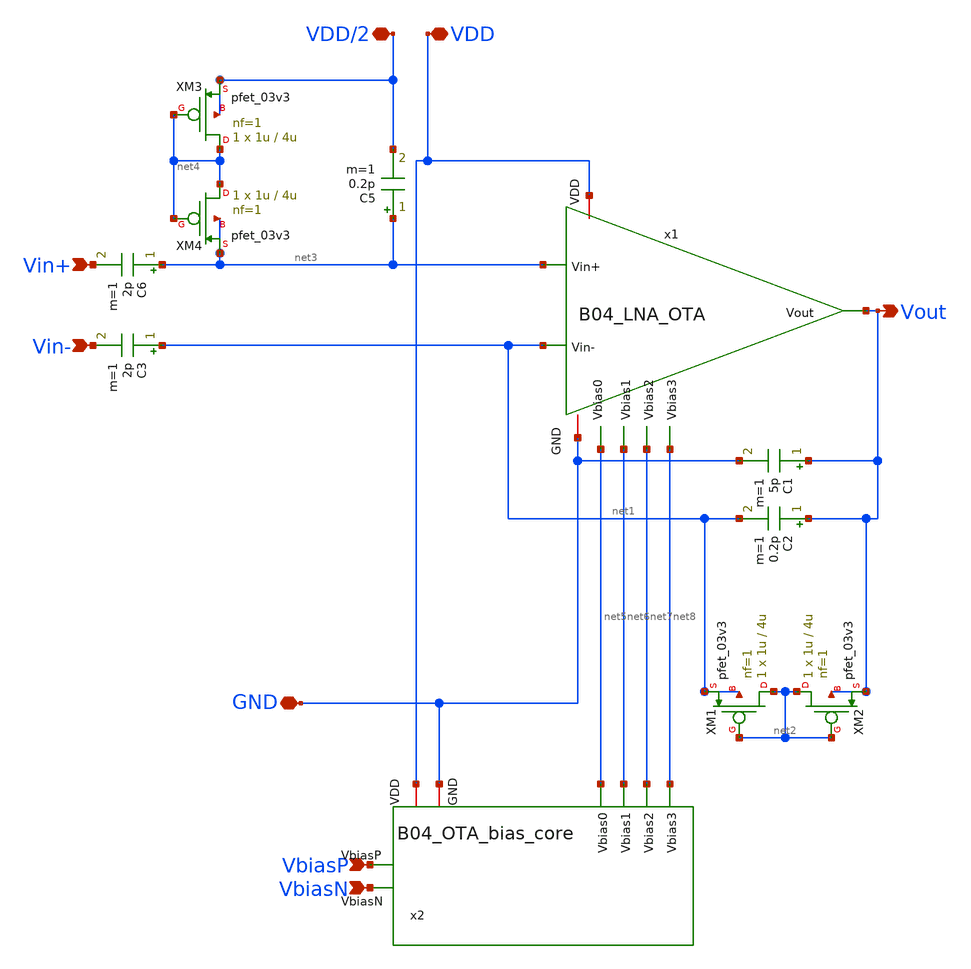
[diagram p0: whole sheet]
** sch_path: analog/B04_LNA.sch
**.subckt B04_LNA VDD VDD/2 GND Vin+ Vin- VbiasP Vout VbiasN
*.iopin VDD
*.iopin VDD/2
*.iopin GND
*.ipin Vin+
*.ipin Vin-
*.ipin VbiasP
*.opin Vout
*.ipin VbiasN
C2 Vout net1 0.2p m=1
C3 net1 Vin- 2p m=1
C5 net3 VDD/2 0.2p m=1
XM1 net2 net2 net1 net1 pfet_03v3 L=4u W=1u nf=1 ad='int((nf+1)/2) * W/nf * 0.18u' as='int((nf+2)/2) * W/nf * 0.18u'
+ pd='2*int((nf+1)/2) * (W/nf + 0.18u)' ps='2*int((nf+2)/2) * (W/nf + 0.18u)' nrd='0.18u / W' nrs='0.18u / W'
+ sa=0 sb=0 sd=0 m=1
XM2 net2 net2 Vout Vout pfet_03v3 L=4u W=1u nf=1 ad='int((nf+1)/2) * W/nf * 0.18u' as='int((nf+2)/2) * W/nf * 0.18u'
+ pd='2*int((nf+1)/2) * (W/nf + 0.18u)' ps='2*int((nf+2)/2) * (W/nf + 0.18u)' nrd='0.18u / W' nrs='0.18u / W'
+ sa=0 sb=0 sd=0 m=1
XM3 net4 net4 VDD/2 VDD/2 pfet_03v3 L=4u W=1u nf=1 ad='int((nf+1)/2) * W/nf * 0.18u' as='int((nf+2)/2) * W/nf * 0.18u'
+ pd='2*int((nf+1)/2) * (W/nf + 0.18u)' ps='2*int((nf+2)/2) * (W/nf + 0.18u)' nrd='0.18u / W' nrs='0.18u / W'
+ sa=0 sb=0 sd=0 m=1
XM4 net4 net4 net3 net3 pfet_03v3 L=4u W=1u nf=1 ad='int((nf+1)/2) * W/nf * 0.18u' as='int((nf+2)/2) * W/nf * 0.18u'
+ pd='2*int((nf+1)/2) * (W/nf + 0.18u)' ps='2*int((nf+2)/2) * (W/nf + 0.18u)' nrd='0.18u / W' nrs='0.18u / W'
+ sa=0 sb=0 sd=0 m=1
C6 net3 Vin+ 2p m=1
x1 VDD net5 net3 net1 net8 net6 Vout net7 GND B04_LNA_OTA
x2 VDD VbiasP net5 net7 net8 net6 VbiasN GND B04_OTA_bias_core ratio=8
C1 Vout GND 5p m=1
**.ends

* expanding   symbol:
*+  AURA-Event-Driven-Mixed-Signal-ASIC-for-Acoustic-Pattern-Detection/analog/B04_LNA_OTA.sym # of pins=9
** sym_path: analog/B04_LNA_OTA.sym
** sch_path: analog/B04_LNA_OTA.sch
.subckt B04_LNA_OTA VDD Vbias0 Vin+ Vin- Vbias3 Vbias1 Vout Vbias2 GND
*.iopin VDD
*.ipin Vbias0
*.ipin Vin+
*.ipin Vin-
*.opin Vout
*.ipin Vbias3
*.ipin Vbias2
*.iopin GND
*.ipin Vbias1
XM1 net1 Vbias0 VDD VDD pfet_03v3 L=4u W=5u nf=2 ad='int((nf+1)/2) * W/nf * 0.18u' as='int((nf+2)/2) * W/nf * 0.18u'
+ pd='2*int((nf+1)/2) * (W/nf + 0.18u)' ps='2*int((nf+2)/2) * (W/nf + 0.18u)' nrd='0.18u / W' nrs='0.18u / W'
+ sa=0 sb=0 sd=0 m=1
XM2 net6 Vin+ net1 VDD pfet_03v3 L=8u W=16u nf=9 ad='int((nf+1)/2) * W/nf * 0.18u' as='int((nf+2)/2) * W/nf * 0.18u'
+ pd='2*int((nf+1)/2) * (W/nf + 0.18u)' ps='2*int((nf+2)/2) * (W/nf + 0.18u)' nrd='0.18u / W' nrs='0.18u / W'
+ sa=0 sb=0 sd=0 m=1
XM3 net7 Vin- net1 VDD pfet_03v3 L=8u W=16u nf=9 ad='int((nf+1)/2) * W/nf * 0.18u' as='int((nf+2)/2) * W/nf * 0.18u'
+ pd='2*int((nf+1)/2) * (W/nf + 0.18u)' ps='2*int((nf+2)/2) * (W/nf + 0.18u)' nrd='0.18u / W' nrs='0.18u / W'
+ sa=0 sb=0 sd=0 m=1
XM4 net2 Vin+ net1 VDD pfet_03v3 L=8u W=16u nf=1 ad='int((nf+1)/2) * W/nf * 0.18u' as='int((nf+2)/2) * W/nf * 0.18u'
+ pd='2*int((nf+1)/2) * (W/nf + 0.18u)' ps='2*int((nf+2)/2) * (W/nf + 0.18u)' nrd='0.18u / W' nrs='0.18u / W'
+ sa=0 sb=0 sd=0 m=1
XM5 net3 Vin- net1 VDD pfet_03v3 L=8u W=16u nf=1 ad='int((nf+1)/2) * W/nf * 0.18u' as='int((nf+2)/2) * W/nf * 0.18u'
+ pd='2*int((nf+1)/2) * (W/nf + 0.18u)' ps='2*int((nf+2)/2) * (W/nf + 0.18u)' nrd='0.18u / W' nrs='0.18u / W'
+ sa=0 sb=0 sd=0 m=1
XM6 net2 Vbias2 net5 0 nfet_03v3 L=2u W=4u nf=1 ad='int((nf+1)/2) * W/nf * 0.18u' as='int((nf+2)/2) * W/nf * 0.18u'
+ pd='2*int((nf+1)/2) * (W/nf + 0.18u)' ps='2*int((nf+2)/2) * (W/nf + 0.18u)' nrd='0.18u / W' nrs='0.18u / W'
+ sa=0 sb=0 sd=0 m=1
XM7 net3 Vbias2 net4 0 nfet_03v3 L=2u W=4u nf=1 ad='int((nf+1)/2) * W/nf * 0.18u' as='int((nf+2)/2) * W/nf * 0.18u'
+ pd='2*int((nf+1)/2) * (W/nf + 0.18u)' ps='2*int((nf+2)/2) * (W/nf + 0.18u)' nrd='0.18u / W' nrs='0.18u / W'
+ sa=0 sb=0 sd=0 m=1
XM8 net5 net2 GND GND nfet_03v3 L=8u W=2u nf=1 ad='int((nf+1)/2) * W/nf * 0.18u' as='int((nf+2)/2) * W/nf * 0.18u'
+ pd='2*int((nf+1)/2) * (W/nf + 0.18u)' ps='2*int((nf+2)/2) * (W/nf + 0.18u)' nrd='0.18u / W' nrs='0.18u / W'
+ sa=0 sb=0 sd=0 m=1
XM9 net6 net3 GND GND nfet_03v3 L=8u W=2u nf=1 ad='int((nf+1)/2) * W/nf * 0.18u' as='int((nf+2)/2) * W/nf * 0.18u'
+ pd='2*int((nf+1)/2) * (W/nf + 0.18u)' ps='2*int((nf+2)/2) * (W/nf + 0.18u)' nrd='0.18u / W' nrs='0.18u / W'
+ sa=0 sb=0 sd=0 m=1
XM10 net4 net3 GND GND nfet_03v3 L=8u W=2u nf=1 ad='int((nf+1)/2) * W/nf * 0.18u' as='int((nf+2)/2) * W/nf * 0.18u'
+ pd='2*int((nf+1)/2) * (W/nf + 0.18u)' ps='2*int((nf+2)/2) * (W/nf + 0.18u)' nrd='0.18u / W' nrs='0.18u / W'
+ sa=0 sb=0 sd=0 m=1
XM11 net7 net2 GND GND nfet_03v3 L=8u W=2u nf=1 ad='int((nf+1)/2) * W/nf * 0.18u' as='int((nf+2)/2) * W/nf * 0.18u'
+ pd='2*int((nf+1)/2) * (W/nf + 0.18u)' ps='2*int((nf+2)/2) * (W/nf + 0.18u)' nrd='0.18u / W' nrs='0.18u / W'
+ sa=0 sb=0 sd=0 m=1
XM12 net9 net10 VDD VDD pfet_03v3 L=8u W=10u nf=1 ad='int((nf+1)/2) * W/nf * 0.18u' as='int((nf+2)/2) * W/nf * 0.18u'
+ pd='2*int((nf+1)/2) * (W/nf + 0.18u)' ps='2*int((nf+2)/2) * (W/nf + 0.18u)' nrd='0.18u / W' nrs='0.18u / W'
+ sa=0 sb=0 sd=0 m=1
XM13 net8 net10 VDD VDD pfet_03v3 L=8u W=10u nf=1 ad='int((nf+1)/2) * W/nf * 0.18u' as='int((nf+2)/2) * W/nf * 0.18u'
+ pd='2*int((nf+1)/2) * (W/nf + 0.18u)' ps='2*int((nf+2)/2) * (W/nf + 0.18u)' nrd='0.18u / W' nrs='0.18u / W'
+ sa=0 sb=0 sd=0 m=1
XM14 Vout Vbias3 net9 VDD pfet_03v3 L=8u W=10u nf=1 ad='int((nf+1)/2) * W/nf * 0.18u' as='int((nf+2)/2) * W/nf * 0.18u'
+ pd='2*int((nf+1)/2) * (W/nf + 0.18u)' ps='2*int((nf+2)/2) * (W/nf + 0.18u)' nrd='0.18u / W' nrs='0.18u / W'
+ sa=0 sb=0 sd=0 m=1
XM15 net10 Vbias3 net8 VDD pfet_03v3 L=8u W=10u nf=1 ad='int((nf+1)/2) * W/nf * 0.18u' as='int((nf+2)/2) * W/nf * 0.18u'
+ pd='2*int((nf+1)/2) * (W/nf + 0.18u)' ps='2*int((nf+2)/2) * (W/nf + 0.18u)' nrd='0.18u / W' nrs='0.18u / W'
+ sa=0 sb=0 sd=0 m=1
XM16 Vout Vbias2 net7 0 nfet_03v3 L=8u W=2u nf=1 ad='int((nf+1)/2) * W/nf * 0.18u' as='int((nf+2)/2) * W/nf * 0.18u'
+ pd='2*int((nf+1)/2) * (W/nf + 0.18u)' ps='2*int((nf+2)/2) * (W/nf + 0.18u)' nrd='0.18u / W' nrs='0.18u / W'
+ sa=0 sb=0 sd=0 m=1
XM17 net10 Vbias2 net6 0 nfet_03v3 L=8u W=2u nf=1 ad='int((nf+1)/2) * W/nf * 0.18u' as='int((nf+2)/2) * W/nf * 0.18u'
+ pd='2*int((nf+1)/2) * (W/nf + 0.18u)' ps='2*int((nf+2)/2) * (W/nf + 0.18u)' nrd='0.18u / W' nrs='0.18u / W'
+ sa=0 sb=0 sd=0 m=1
XM18 net6 Vbias1 GND GND nfet_03v3 L=8u W=2u nf=10 ad='int((nf+1)/2) * W/nf * 0.18u' as='int((nf+2)/2) * W/nf * 0.18u'
+ pd='2*int((nf+1)/2) * (W/nf + 0.18u)' ps='2*int((nf+2)/2) * (W/nf + 0.18u)' nrd='0.18u / W' nrs='0.18u / W'
+ sa=0 sb=0 sd=0 m=1
XM19 net7 Vbias1 GND GND nfet_03v3 L=8u W=2u nf=10 ad='int((nf+1)/2) * W/nf * 0.18u' as='int((nf+2)/2) * W/nf * 0.18u'
+ pd='2*int((nf+1)/2) * (W/nf + 0.18u)' ps='2*int((nf+2)/2) * (W/nf + 0.18u)' nrd='0.18u / W' nrs='0.18u / W'
+ sa=0 sb=0 sd=0 m=1
.ends


* expanding   symbol:
*+  AURA-Event-Driven-Mixed-Signal-ASIC-for-Acoustic-Pattern-Detection/analog/B04_OTA_bias_core.sym # of pins=8
** sym_path: analog/B04_OTA_bias_core.sym
** sch_path: analog/B04_OTA_bias_core.sch
.subckt B04_OTA_bias_core VDD VbiasP Vbias0 Vbias2 Vbias3 Vbias1 VbiasN GND  ratio=1
*.iopin VDD
*.opin Vbias2
*.opin Vbias1
*.opin Vbias0
*.opin Vbias3
*.iopin GND
*.ipin VbiasP
*.ipin VbiasN
XM1 Vbias1 GND Vbias2 VDD pfet_03v3 L=4u W=5u nf=1 ad='int((nf+1)/2) * W/nf * 0.18u' as='int((nf+2)/2) * W/nf * 0.18u'
+ pd='2*int((nf+1)/2) * (W/nf + 0.18u)' ps='2*int((nf+2)/2) * (W/nf + 0.18u)' nrd='0.18u / W' nrs='0.18u / W'
+ sa=0 sb=0 sd=0 m=1
XM4 Vbias1 Vbias2 net1 GND nfet_03v3 L=4u W=1u nf=1 ad='int((nf+1)/2) * W/nf * 0.18u' as='int((nf+2)/2) * W/nf * 0.18u'
+ pd='2*int((nf+1)/2) * (W/nf + 0.18u)' ps='2*int((nf+2)/2) * (W/nf + 0.18u)' nrd='0.18u / W' nrs='0.18u / W'
+ sa=0 sb=0 sd=0 m=1
XM5 net1 Vbias1 GND GND nfet_03v3 L=4u W=1u nf=1 ad='int((nf+1)/2) * W/nf * 0.18u' as='int((nf+2)/2) * W/nf * 0.18u'
+ pd='2*int((nf+1)/2) * (W/nf + 0.18u)' ps='2*int((nf+2)/2) * (W/nf + 0.18u)' nrd='0.18u / W' nrs='0.18u / W'
+ sa=0 sb=0 sd=0 m=1
XM9 net2 Vbias3 Vbias0 VDD pfet_03v3 L=4u W=5u nf=1 ad='int((nf+1)/2) * W/nf * 0.18u' as='int((nf+2)/2) * W/nf * 0.18u'
+ pd='2*int((nf+1)/2) * (W/nf + 0.18u)' ps='2*int((nf+2)/2) * (W/nf + 0.18u)' nrd='0.18u / W' nrs='0.18u / W'
+ sa=0 sb=0 sd=0 m=1
XM10 VDD Vbias0 net2 VDD pfet_03v3 L=4u W=5u nf=1 ad='int((nf+1)/2) * W/nf * 0.18u' as='int((nf+2)/2) * W/nf * 0.18u'
+ pd='2*int((nf+1)/2) * (W/nf + 0.18u)' ps='2*int((nf+2)/2) * (W/nf + 0.18u)' nrd='0.18u / W' nrs='0.18u / W'
+ sa=0 sb=0 sd=0 m=1
XM6 Vbias3 VDD Vbias0 GND nfet_03v3 L=4u W=10u nf=1 ad='int((nf+1)/2) * W/nf * 0.18u' as='int((nf+2)/2) * W/nf * 0.18u'
+ pd='2*int((nf+1)/2) * (W/nf + 0.18u)' ps='2*int((nf+2)/2) * (W/nf + 0.18u)' nrd='0.18u / W' nrs='0.18u / W'
+ sa=0 sb=0 sd=0 m=1
XM2 Vbias2 VbiasP VDD VDD pfet_03v3 L=4u W={ratio*2u} nf=1 ad='int((nf+1)/2) * W/nf * 0.18u' as='int((nf+2)/2) * W/nf * 0.18u'
+ pd='2*int((nf+1)/2) * (W/nf + 0.18u)' ps='2*int((nf+2)/2) * (W/nf + 0.18u)' nrd='0.18u / W' nrs='0.18u / W'
+ sa=0 sb=0 sd=0 m=1
XM3 GND VbiasN Vbias3 GND nfet_03v3 L=4u W={ratio*10u} nf=1 ad='int((nf+1)/2) * W/nf * 0.18u' as='int((nf+2)/2) * W/nf * 0.18u'
+ pd='2*int((nf+1)/2) * (W/nf + 0.18u)' ps='2*int((nf+2)/2) * (W/nf + 0.18u)' nrd='0.18u / W' nrs='0.18u / W'
+ sa=0 sb=0 sd=0 m=1
.ends

.end
